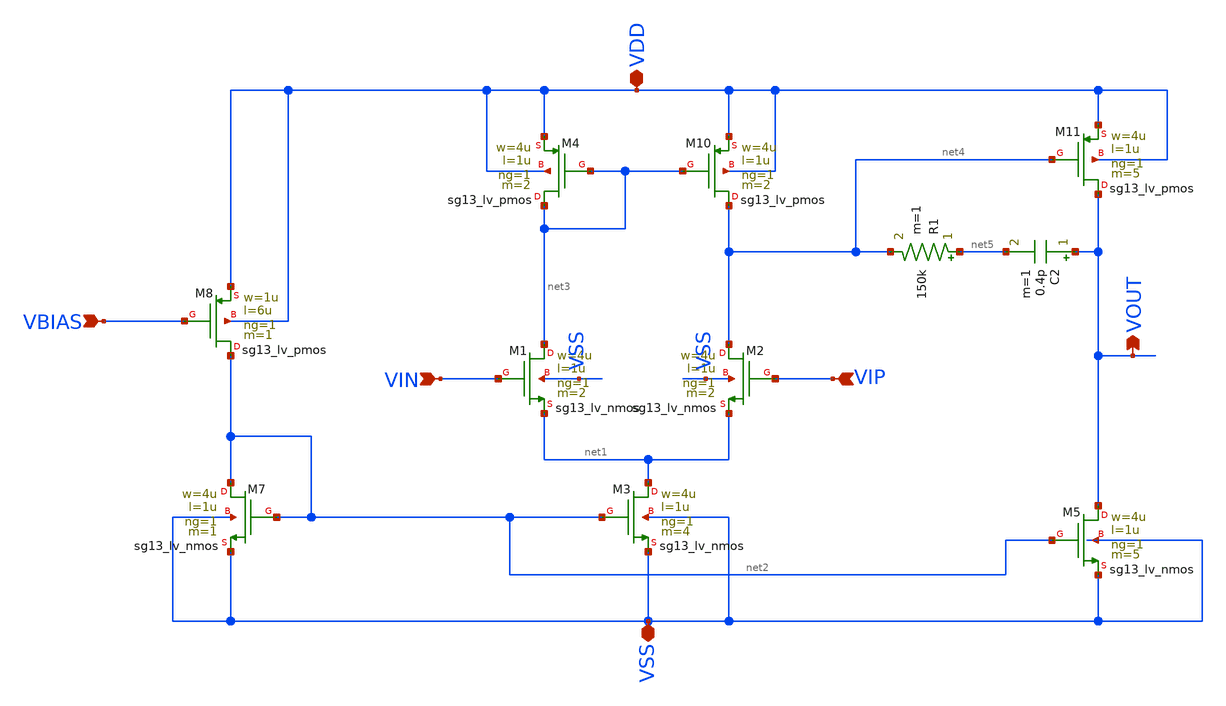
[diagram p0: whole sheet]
** sch_path: BTDay5-Ex/2-stageOpampWithoutCMFB.sch
**.subckt 2-stageOpampWithoutCMFB VSS VDD VIP VIN VBIAS VOUT
*.iopin VSS
*.iopin VDD
*.ipin VIP
*.ipin VIN
*.ipin VBIAS
*.opin VOUT
XM1 net3 VIN net1 VSS sg13_lv_nmos w=4u l=1u ng=1 m=2 mm_ok=1
XM2 net4 VIP net1 VSS sg13_lv_nmos w=4u l=1u ng=1 m=2 mm_ok=1
XM3 net1 net2 VSS VSS sg13_lv_nmos w=4u l=1u ng=1 m=4 mm_ok=1
XM4 net3 net3 VDD VDD sg13_lv_pmos w=4u l=1u ng=1 m=2 mm_ok=1
XM7 net2 net2 VSS VSS sg13_lv_nmos w=4u l=1u ng=1 m=1 mm_ok=1
XM8 net2 VBIAS VDD VDD sg13_lv_pmos w=1u l=6u ng=1 m=1 mm_ok=1
XM10 net4 net3 VDD VDD sg13_lv_pmos w=4u l=1u ng=1 m=2 mm_ok=1
XM5 VOUT net2 VSS VSS sg13_lv_nmos w=4u l=1u ng=1 m=5 mm_ok=1
XM11 VOUT net4 VDD VDD sg13_lv_pmos w=4u l=1u ng=1 m=5 mm_ok=1
C2 VOUT net5 0.4p m=1
R1 net5 net4 150k m=1
**.ends
.end
